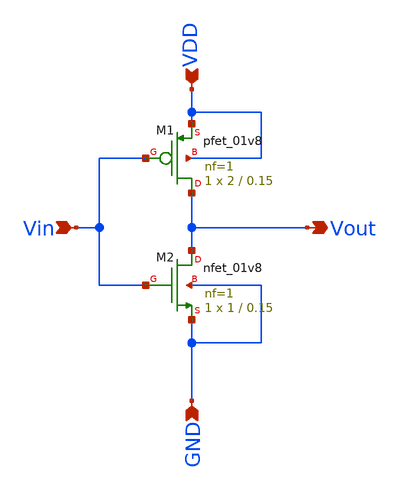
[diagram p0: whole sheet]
** sch_path: Invert2.sch
**.subckt Invert2 VDD Vin GND Vout
*.ipin VDD
*.ipin Vin
*.ipin GND
*.opin Vout
XM1 Vout Vin VDD VDD sky130_fd_pr__pfet_01v8 L=0.15 W=2 nf=1 ad='int((1 + 1)/2) * 2 / 1 * 0.29' as='int((1 + 2)/2) * 2 / 1 * 0.29'
+ pd='2*int((1 + 1)/2) * (2 / 1 + 0.29)' ps='2*int((1 + 2)/2) * (2 / 1 + 0.29)' nrd='0.29 / 2 ' nrs='0.29 / 2 '
+ sa=0 sb=0 sd=0 mult=1 m=1
XM2 Vout Vin GND GND sky130_fd_pr__nfet_01v8 L=0.15 W=1 nf=1 ad='int((1 + 1)/2) * 1 / 1 * 0.29' as='int((1 + 2)/2) * 1 / 1 * 0.29'
+ pd='2*int((1 + 1)/2) * (1 / 1 + 0.29)' ps='2*int((1 + 2)/2) * (1 / 1 + 0.29)' nrd='0.29 / 1 ' nrs='0.29 / 1 '
+ sa=0 sb=0 sd=0 mult=1 m=1
**.ends
.end
